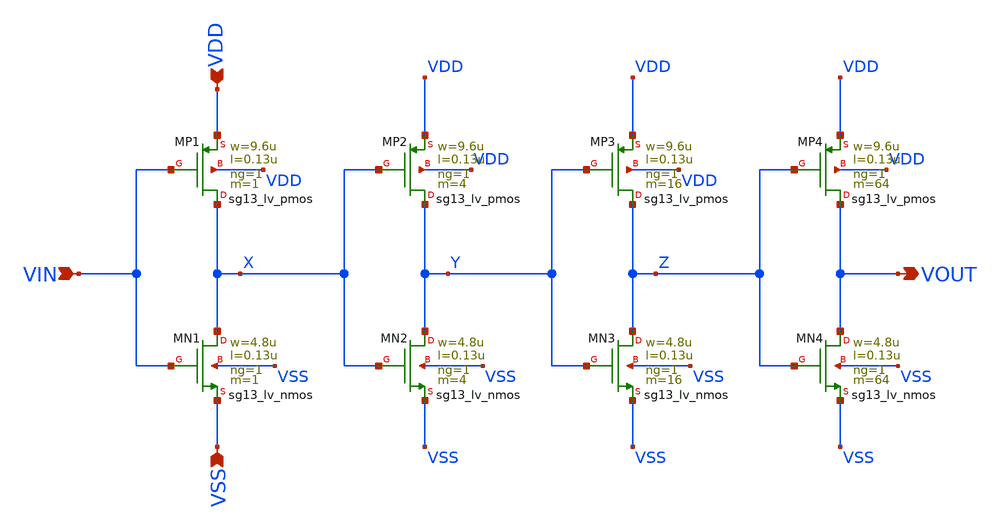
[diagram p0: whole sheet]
** sch_path: OSC9996-main/schematic/xschem/gate_buff_pad.sch
**.subckt gate_buff_pad VDD VIN VSS VOUT
*.ipin VDD
*.ipin VIN
*.ipin VSS
*.opin VOUT
XMN1 X VIN VSS VSS sg13_lv_nmos w=4.8u l=0.13u ng=1 m=1 mm_ok=1
XMP1 X VIN VDD VDD sg13_lv_pmos w=9.6u l=0.13u ng=1 m=1 mm_ok=1
XMN2 Y X VSS VSS sg13_lv_nmos w=4.8u l=0.13u ng=1 m=4 mm_ok=1
XMP2 Y X VDD VDD sg13_lv_pmos w=9.6u l=0.13u ng=1 m=4 mm_ok=1
XMN3 Z Y VSS VSS sg13_lv_nmos w=4.8u l=0.13u ng=1 m=16 mm_ok=1
XMP3 Z Y VDD VDD sg13_lv_pmos w=9.6u l=0.13u ng=1 m=16 mm_ok=1
XMN4 VOUT Z VSS VSS sg13_lv_nmos w=4.8u l=0.13u ng=1 m=64 mm_ok=1
XMP4 VOUT Z VDD VDD sg13_lv_pmos w=9.6u l=0.13u ng=1 m=64 mm_ok=1
**.ends
.end
